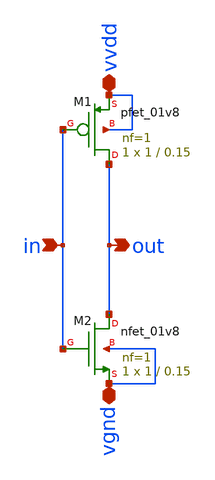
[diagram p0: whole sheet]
** sch_path: ringoscilator/inverterspice.sch
**.subckt inverterspice in out vvdd vgnd
*.ipin in
*.opin out
*.iopin vvdd
*.iopin vgnd
XM1 out in vvdd vvdd sky130_fd_pr__pfet_01v8 L=0.15 W=1 nf=1 ad='int((nf+1)/2) * W/nf * 0.29' as='int((nf+2)/2) * W/nf * 0.29'
+ pd='2*int((nf+1)/2) * (W/nf + 0.29)' ps='2*int((nf+2)/2) * (W/nf + 0.29)' nrd='0.29 / W' nrs='0.29 / W'
+ sa=0 sb=0 sd=0 mult=1 m=1
XM2 out in vgnd vgnd sky130_fd_pr__nfet_01v8 L=0.15 W=1 nf=1 ad='int((nf+1)/2) * W/nf * 0.29' as='int((nf+2)/2) * W/nf * 0.29'
+ pd='2*int((nf+1)/2) * (W/nf + 0.29)' ps='2*int((nf+2)/2) * (W/nf + 0.29)' nrd='0.29 / W' nrs='0.29 / W'
+ sa=0 sb=0 sd=0 mult=1 m=1
**.ends
.end
